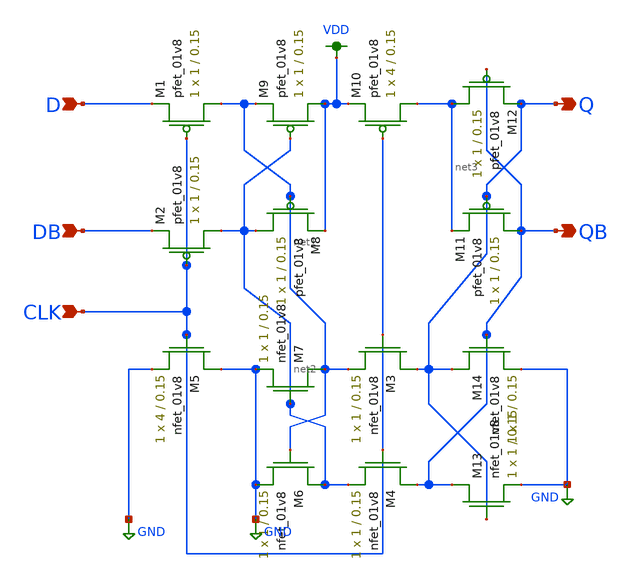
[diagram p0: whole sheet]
** sch_path: MP2/DFF_LDS.sch
**.subckt DFF_LDS D DB CLK Q QB
*.ipin D
*.ipin DB
*.ipin CLK
*.opin Q
*.opin QB
XM1 net1 CLK D VDD sky130_fd_pr__pfet_01v8 L=0.15 W=1 nf=1 ad='int((nf+1)/2) * W/nf * 0.29' as='int((nf+2)/2) * W/nf * 0.29'
+ pd='2*int((nf+1)/2) * (W/nf + 0.29)' ps='2*int((nf+2)/2) * (W/nf + 0.29)' nrd='0.29 / W' nrs='0.29 / W'
+ sa=0 sb=0 sd=0 mult=1 m=1
XM2 net2 CLK DB VDD sky130_fd_pr__pfet_01v8 L=0.15 W=1 nf=1 ad='int((nf+1)/2) * W/nf * 0.29' as='int((nf+2)/2) * W/nf * 0.29'
+ pd='2*int((nf+1)/2) * (W/nf + 0.29)' ps='2*int((nf+2)/2) * (W/nf + 0.29)' nrd='0.29 / W' nrs='0.29 / W'
+ sa=0 sb=0 sd=0 mult=1 m=1
XM3 Q CLK net1 GND sky130_fd_pr__nfet_01v8 L=0.15 W=1 nf=1 ad='int((nf+1)/2) * W/nf * 0.29' as='int((nf+2)/2) * W/nf * 0.29'
+ pd='2*int((nf+1)/2) * (W/nf + 0.29)' ps='2*int((nf+2)/2) * (W/nf + 0.29)' nrd='0.29 / W' nrs='0.29 / W'
+ sa=0 sb=0 sd=0 mult=1 m=1
XM4 QB CLK net2 GND sky130_fd_pr__nfet_01v8 L=0.15 W=1 nf=1 ad='int((nf+1)/2) * W/nf * 0.29' as='int((nf+2)/2) * W/nf * 0.29'
+ pd='2*int((nf+1)/2) * (W/nf + 0.29)' ps='2*int((nf+2)/2) * (W/nf + 0.29)' nrd='0.29 / W' nrs='0.29 / W'
+ sa=0 sb=0 sd=0 mult=1 m=1
XM5 GND CLK GND GND sky130_fd_pr__nfet_01v8 L=0.15 W=4 nf=1 ad='int((nf+1)/2) * W/nf * 0.29' as='int((nf+2)/2) * W/nf * 0.29'
+ pd='2*int((nf+1)/2) * (W/nf + 0.29)' ps='2*int((nf+2)/2) * (W/nf + 0.29)' nrd='0.29 / W' nrs='0.29 / W'
+ sa=0 sb=0 sd=0 mult=1 m=1
XM6 net2 net1 GND GND sky130_fd_pr__nfet_01v8 L=0.15 W=1 nf=1 ad='int((nf+1)/2) * W/nf * 0.29' as='int((nf+2)/2) * W/nf * 0.29'
+ pd='2*int((nf+1)/2) * (W/nf + 0.29)' ps='2*int((nf+2)/2) * (W/nf + 0.29)' nrd='0.29 / W' nrs='0.29 / W'
+ sa=0 sb=0 sd=0 mult=1 m=1
XM7 net1 net2 GND GND sky130_fd_pr__nfet_01v8 L=0.15 W=1 nf=1 ad='int((nf+1)/2) * W/nf * 0.29' as='int((nf+2)/2) * W/nf * 0.29'
+ pd='2*int((nf+1)/2) * (W/nf + 0.29)' ps='2*int((nf+2)/2) * (W/nf + 0.29)' nrd='0.29 / W' nrs='0.29 / W'
+ sa=0 sb=0 sd=0 mult=1 m=1
XM8 net2 net1 VDD VDD sky130_fd_pr__pfet_01v8 L=0.15 W=1 nf=1 ad='int((nf+1)/2) * W/nf * 0.29' as='int((nf+2)/2) * W/nf * 0.29'
+ pd='2*int((nf+1)/2) * (W/nf + 0.29)' ps='2*int((nf+2)/2) * (W/nf + 0.29)' nrd='0.29 / W' nrs='0.29 / W'
+ sa=0 sb=0 sd=0 mult=1 m=1
XM9 VDD net2 net1 VDD sky130_fd_pr__pfet_01v8 L=0.15 W=1 nf=1 ad='int((nf+1)/2) * W/nf * 0.29' as='int((nf+2)/2) * W/nf * 0.29'
+ pd='2*int((nf+1)/2) * (W/nf + 0.29)' ps='2*int((nf+2)/2) * (W/nf + 0.29)' nrd='0.29 / W' nrs='0.29 / W'
+ sa=0 sb=0 sd=0 mult=1 m=1
XM10 net3 CLK VDD VDD sky130_fd_pr__pfet_01v8 L=0.15 W=4 nf=1 ad='int((nf+1)/2) * W/nf * 0.29' as='int((nf+2)/2) * W/nf * 0.29'
+ pd='2*int((nf+1)/2) * (W/nf + 0.29)' ps='2*int((nf+2)/2) * (W/nf + 0.29)' nrd='0.29 / W' nrs='0.29 / W'
+ sa=0 sb=0 sd=0 mult=1 m=1
XM11 QB Q net3 VDD sky130_fd_pr__pfet_01v8 L=0.15 W=1 nf=1 ad='int((nf+1)/2) * W/nf * 0.29' as='int((nf+2)/2) * W/nf * 0.29'
+ pd='2*int((nf+1)/2) * (W/nf + 0.29)' ps='2*int((nf+2)/2) * (W/nf + 0.29)' nrd='0.29 / W' nrs='0.29 / W'
+ sa=0 sb=0 sd=0 mult=1 m=1
XM12 net3 QB Q VDD sky130_fd_pr__pfet_01v8 L=0.15 W=1 nf=1 ad='int((nf+1)/2) * W/nf * 0.29' as='int((nf+2)/2) * W/nf * 0.29'
+ pd='2*int((nf+1)/2) * (W/nf + 0.29)' ps='2*int((nf+2)/2) * (W/nf + 0.29)' nrd='0.29 / W' nrs='0.29 / W'
+ sa=0 sb=0 sd=0 mult=1 m=1
XM13 QB Q GND GND sky130_fd_pr__nfet_01v8 L=0.15 W=1 nf=1 ad='int((nf+1)/2) * W/nf * 0.29' as='int((nf+2)/2) * W/nf * 0.29'
+ pd='2*int((nf+1)/2) * (W/nf + 0.29)' ps='2*int((nf+2)/2) * (W/nf + 0.29)' nrd='0.29 / W' nrs='0.29 / W'
+ sa=0 sb=0 sd=0 mult=1 m=1
XM14 Q QB GND GND sky130_fd_pr__nfet_01v8 L=0.15 W=1 nf=1 ad='int((nf+1)/2) * W/nf * 0.29' as='int((nf+2)/2) * W/nf * 0.29'
+ pd='2*int((nf+1)/2) * (W/nf + 0.29)' ps='2*int((nf+2)/2) * (W/nf + 0.29)' nrd='0.29 / W' nrs='0.29 / W'
+ sa=0 sb=0 sd=0 mult=1 m=1
**.ends
.GLOBAL VDD
.GLOBAL GND
.end
